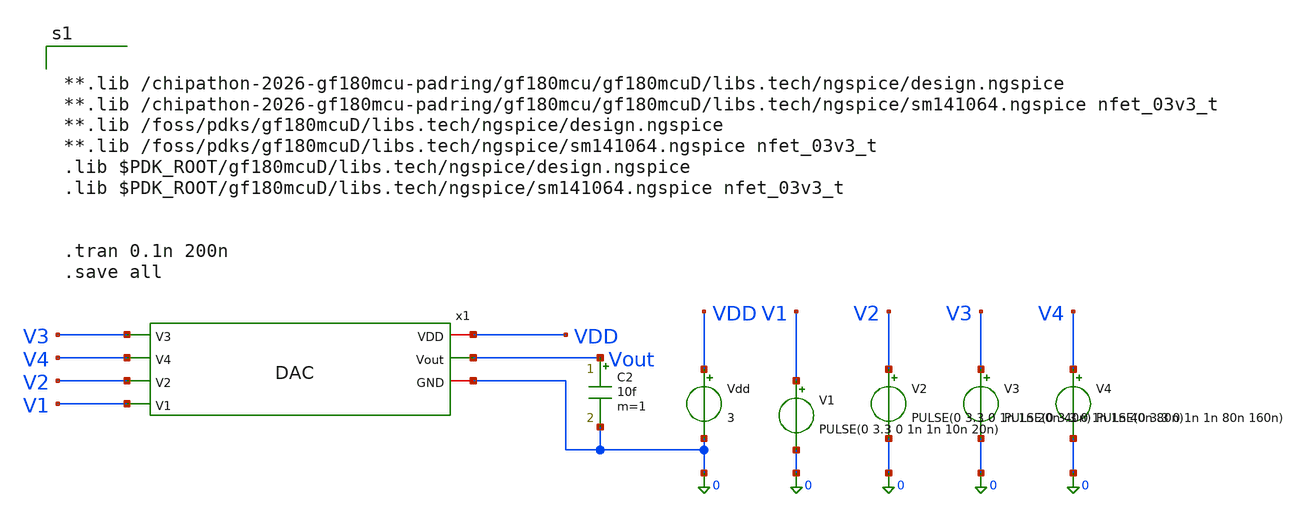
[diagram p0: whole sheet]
** sch_path: src/schematic/DAC/dac_tb.sch
**.subckt dac_tb
Vdd VDD 0 3
V1 V1 0 PULSE(0 3.3 0 1n 1n 10n 20n)
V2 V2 0 PULSE(0 3.3 0 1n 1n 20n 40n)
V3 V3 0 PULSE(0 3.3 0 1n 1n 40n 80n)
V4 V4 0 PULSE(0 3.3 0 1n 1n 80n 160n)
x1 VDD Vout 0 V3 V4 V2 V1 dac
C2 Vout 0 10f m=1
**** begin user architecture code


**.lib /chipathon-2026-gf180mcu-padring/gf180mcu/gf180mcuD/libs.tech/ngspice/design.ngspice
**.lib /chipathon-2026-gf180mcu-padring/gf180mcu/gf180mcuD/libs.tech/ngspice/sm141064.ngspice nfet_03v3_t
**.lib /foss/pdks/gf180mcuD/libs.tech/ngspice/design.ngspice
**.lib /foss/pdks/gf180mcuD/libs.tech/ngspice/sm141064.ngspice nfet_03v3_t
.lib $PDK_ROOT/gf180mcuD/libs.tech/ngspice/design.ngspice
.lib $PDK_ROOT/gf180mcuD/libs.tech/ngspice/sm141064.ngspice nfet_03v3_t


.tran 0.1n 200n
.save all


**** end user architecture code
**.ends

* expanding   symbol:  src/schematic/DAC/dac.sym # of pins=7
** sym_path: src/schematic/DAC/dac.sym
** sch_path: src/schematic/DAC/dac.sch
.subckt dac VDD Vout GND V3 V4 V2 V1
*.ipin V1
*.ipin V2
*.ipin V3
*.ipin V4
*.opin Vout
*.iopin VDD
*.iopin GND
R1 VDD Vout 1k m=1
R2 VDD net3 1k m=1
XQ1 net1 net3 V4 V4 nfet_03v3 L=0.28u W=1u nf=1 ad='int((nf+1)/2) * W/nf * 0.18u' as='int((nf+2)/2) * W/nf * 0.18u'
+ pd='2*int((nf+1)/2) * (W/nf + 0.18u)' ps='2*int((nf+2)/2) * (W/nf + 0.18u)' nrd='0.18u / W' nrs='0.18u / W'
+ sa=0 sb=0 sd=0 m=1
XQ2 net4 net3 V4 V4 nfet_03v3 L=0.28u W=2u nf=1 ad='int((nf+1)/2) * W/nf * 0.18u' as='int((nf+2)/2) * W/nf * 0.18u'
+ pd='2*int((nf+1)/2) * (W/nf + 0.18u)' ps='2*int((nf+2)/2) * (W/nf + 0.18u)' nrd='0.18u / W' nrs='0.18u / W'
+ sa=0 sb=0 sd=0 m=1
XQ3 net5 net3 V4 V4 nfet_03v3 L=0.28u W=4u nf=1 ad='int((nf+1)/2) * W/nf * 0.18u' as='int((nf+2)/2) * W/nf * 0.18u'
+ pd='2*int((nf+1)/2) * (W/nf + 0.18u)' ps='2*int((nf+2)/2) * (W/nf + 0.18u)' nrd='0.18u / W' nrs='0.18u / W'
+ sa=0 sb=0 sd=0 m=1
XQ4 net2 net3 V4 V4 nfet_03v3 L=0.28u W=8u nf=1 ad='int((nf+1)/2) * W/nf * 0.18u' as='int((nf+2)/2) * W/nf * 0.18u'
+ pd='2*int((nf+1)/2) * (W/nf + 0.18u)' ps='2*int((nf+2)/2) * (W/nf + 0.18u)' nrd='0.18u / W' nrs='0.18u / W'
+ sa=0 sb=0 sd=0 m=1
XQ0 V4 net3 net3 V4 nfet_03v3 L=0.28u W=1u nf=1 ad='int((nf+1)/2) * W/nf * 0.18u' as='int((nf+2)/2) * W/nf * 0.18u'
+ pd='2*int((nf+1)/2) * (W/nf + 0.18u)' ps='2*int((nf+2)/2) * (W/nf + 0.18u)' nrd='0.18u / W' nrs='0.18u / W'
+ sa=0 sb=0 sd=0 m=1
XTGN1 Vout V1 net1 V4 nfet_03v3 L=0.28u W=5u nf=1 ad='int((nf+1)/2) * W/nf * 0.18u' as='int((nf+2)/2) * W/nf * 0.18u'
+ pd='2*int((nf+1)/2) * (W/nf + 0.18u)' ps='2*int((nf+2)/2) * (W/nf + 0.18u)' nrd='0.18u / W' nrs='0.18u / W'
+ sa=0 sb=0 sd=0 m=1
XTGN2 Vout V2 net4 V4 nfet_03v3 L=0.28u W=5u nf=1 ad='int((nf+1)/2) * W/nf * 0.18u' as='int((nf+2)/2) * W/nf * 0.18u'
+ pd='2*int((nf+1)/2) * (W/nf + 0.18u)' ps='2*int((nf+2)/2) * (W/nf + 0.18u)' nrd='0.18u / W' nrs='0.18u / W'
+ sa=0 sb=0 sd=0 m=1
XTGN3 Vout V3 net5 V4 nfet_03v3 L=0.28u W=5u nf=1 ad='int((nf+1)/2) * W/nf * 0.18u' as='int((nf+2)/2) * W/nf * 0.18u'
+ pd='2*int((nf+1)/2) * (W/nf + 0.18u)' ps='2*int((nf+2)/2) * (W/nf + 0.18u)' nrd='0.18u / W' nrs='0.18u / W'
+ sa=0 sb=0 sd=0 m=1
XTGN4 Vout V4 net2 V4 nfet_03v3 L=0.28u W=5u nf=1 ad='int((nf+1)/2) * W/nf * 0.18u' as='int((nf+2)/2) * W/nf * 0.18u'
+ pd='2*int((nf+1)/2) * (W/nf + 0.18u)' ps='2*int((nf+2)/2) * (W/nf + 0.18u)' nrd='0.18u / W' nrs='0.18u / W'
+ sa=0 sb=0 sd=0 m=1
XTGP1 net1 VB1 Vout VDD pfet_03v3 L=0.28u W=10u nf=1 ad='int((nf+1)/2) * W/nf * 0.18u' as='int((nf+2)/2) * W/nf * 0.18u'
+ pd='2*int((nf+1)/2) * (W/nf + 0.18u)' ps='2*int((nf+2)/2) * (W/nf + 0.18u)' nrd='0.18u / W' nrs='0.18u / W'
+ sa=0 sb=0 sd=0 m=1
XIN1 VB1 V1 V4 V4 nfet_03v3 L=0.28u W=1u nf=1 ad='int((nf+1)/2) * W/nf * 0.18u' as='int((nf+2)/2) * W/nf * 0.18u'
+ pd='2*int((nf+1)/2) * (W/nf + 0.18u)' ps='2*int((nf+2)/2) * (W/nf + 0.18u)' nrd='0.18u / W' nrs='0.18u / W'
+ sa=0 sb=0 sd=0 m=1
XIP1 VB1 V1 VDD VDD pfet_03v3 L=0.28u W=2u nf=1 ad='int((nf+1)/2) * W/nf * 0.18u' as='int((nf+2)/2) * W/nf * 0.18u'
+ pd='2*int((nf+1)/2) * (W/nf + 0.18u)' ps='2*int((nf+2)/2) * (W/nf + 0.18u)' nrd='0.18u / W' nrs='0.18u / W'
+ sa=0 sb=0 sd=0 m=1
XIN2 VB2 V2 V4 V4 nfet_03v3 L=0.28u W=1u nf=1 ad='int((nf+1)/2) * W/nf * 0.18u' as='int((nf+2)/2) * W/nf * 0.18u'
+ pd='2*int((nf+1)/2) * (W/nf + 0.18u)' ps='2*int((nf+2)/2) * (W/nf + 0.18u)' nrd='0.18u / W' nrs='0.18u / W'
+ sa=0 sb=0 sd=0 m=1
XIP2 VB2 V2 VDD VDD pfet_03v3 L=0.28u W=2u nf=1 ad='int((nf+1)/2) * W/nf * 0.18u' as='int((nf+2)/2) * W/nf * 0.18u'
+ pd='2*int((nf+1)/2) * (W/nf + 0.18u)' ps='2*int((nf+2)/2) * (W/nf + 0.18u)' nrd='0.18u / W' nrs='0.18u / W'
+ sa=0 sb=0 sd=0 m=1
XIN3 VB3 V3 V4 V4 nfet_03v3 L=0.28u W=1u nf=1 ad='int((nf+1)/2) * W/nf * 0.18u' as='int((nf+2)/2) * W/nf * 0.18u'
+ pd='2*int((nf+1)/2) * (W/nf + 0.18u)' ps='2*int((nf+2)/2) * (W/nf + 0.18u)' nrd='0.18u / W' nrs='0.18u / W'
+ sa=0 sb=0 sd=0 m=1
XIP3 VB3 V3 VDD VDD pfet_03v3 L=0.28u W=2u nf=1 ad='int((nf+1)/2) * W/nf * 0.18u' as='int((nf+2)/2) * W/nf * 0.18u'
+ pd='2*int((nf+1)/2) * (W/nf + 0.18u)' ps='2*int((nf+2)/2) * (W/nf + 0.18u)' nrd='0.18u / W' nrs='0.18u / W'
+ sa=0 sb=0 sd=0 m=1
XIN4 VB4 V4 V4 V4 nfet_03v3 L=0.28u W=1u nf=1 ad='int((nf+1)/2) * W/nf * 0.18u' as='int((nf+2)/2) * W/nf * 0.18u'
+ pd='2*int((nf+1)/2) * (W/nf + 0.18u)' ps='2*int((nf+2)/2) * (W/nf + 0.18u)' nrd='0.18u / W' nrs='0.18u / W'
+ sa=0 sb=0 sd=0 m=1
XIP4 VB4 V4 VDD VDD pfet_03v3 L=0.28u W=2u nf=1 ad='int((nf+1)/2) * W/nf * 0.18u' as='int((nf+2)/2) * W/nf * 0.18u'
+ pd='2*int((nf+1)/2) * (W/nf + 0.18u)' ps='2*int((nf+2)/2) * (W/nf + 0.18u)' nrd='0.18u / W' nrs='0.18u / W'
+ sa=0 sb=0 sd=0 m=1
XTGP2 net4 VB2 Vout VDD pfet_03v3 L=0.28u W=10u nf=1 ad='int((nf+1)/2) * W/nf * 0.18u' as='int((nf+2)/2) * W/nf * 0.18u'
+ pd='2*int((nf+1)/2) * (W/nf + 0.18u)' ps='2*int((nf+2)/2) * (W/nf + 0.18u)' nrd='0.18u / W' nrs='0.18u / W'
+ sa=0 sb=0 sd=0 m=1
XTGP3 net5 VB3 Vout VDD pfet_03v3 L=0.28u W=10u nf=1 ad='int((nf+1)/2) * W/nf * 0.18u' as='int((nf+2)/2) * W/nf * 0.18u'
+ pd='2*int((nf+1)/2) * (W/nf + 0.18u)' ps='2*int((nf+2)/2) * (W/nf + 0.18u)' nrd='0.18u / W' nrs='0.18u / W'
+ sa=0 sb=0 sd=0 m=1
XTGP4 net2 VB4 Vout VDD pfet_03v3 L=0.28u W=10u nf=1 ad='int((nf+1)/2) * W/nf * 0.18u' as='int((nf+2)/2) * W/nf * 0.18u'
+ pd='2*int((nf+1)/2) * (W/nf + 0.18u)' ps='2*int((nf+2)/2) * (W/nf + 0.18u)' nrd='0.18u / W' nrs='0.18u / W'
+ sa=0 sb=0 sd=0 m=1
.ends

.end
